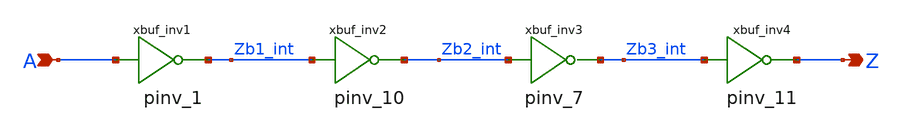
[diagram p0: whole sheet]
** sch_path: sram_2_64_scn4m/pdriver_2.sch
**.subckt pdriver_2 A Z
*.ipin A
*.opin Z
xbuf_inv1 A Zb1_int vdd gnd pinv_1
xbuf_inv2 Zb1_int Zb2_int vdd gnd pinv_10
xbuf_inv3 Zb2_int Zb3_int vdd gnd pinv_7
xbuf_inv4 Zb3_int Z gnd gnd pinv_11
**.ends
.end
